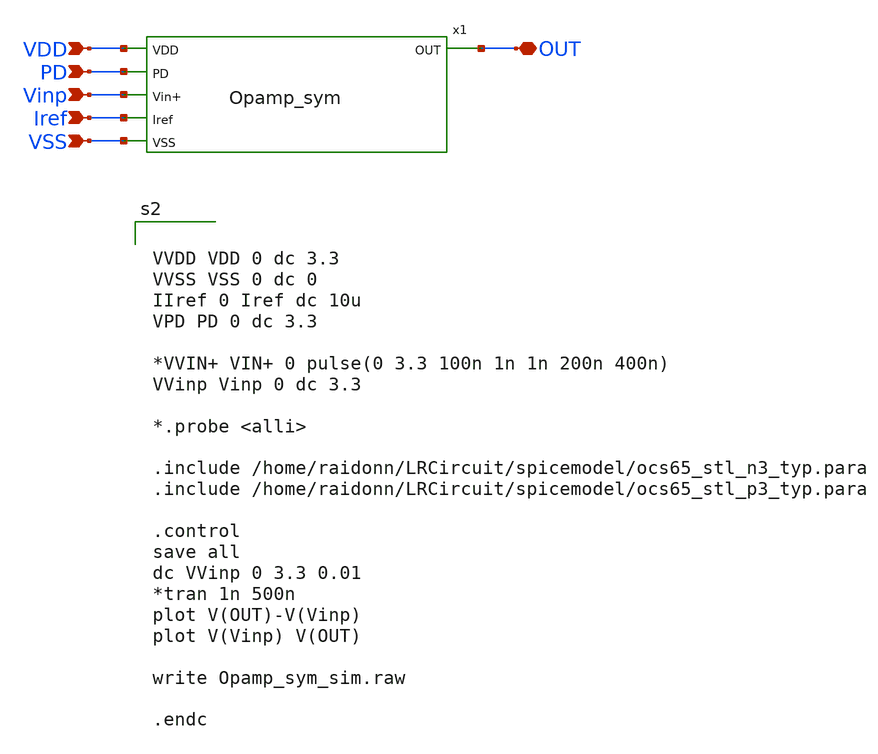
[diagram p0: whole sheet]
** sch_path: LR_Work4/Review_1112/sim/Opamp_sym_sim.sch
**.subckt Opamp_sym_sim VDD PD Vinp Iref VSS OUT
*.ipin VDD
*.ipin PD
*.ipin Vinp
*.ipin Iref
*.ipin VSS
*.iopin OUT
x1 VDD PD Vinp Iref VSS OUT Opamp_sym
**** begin user architecture code


VVDD VDD 0 dc 3.3
VVSS VSS 0 dc 0
IIref 0 Iref dc 10u
VPD PD 0 dc 3.3

*VVIN+ VIN+ 0 pulse(0 3.3 100n 1n 1n 200n 400n)
VVinp Vinp 0 dc 3.3

*.probe <alli>

.include /home/raidonn/LRCircuit/spicemodel/ocs65_stl_n3_typ.para
.include /home/raidonn/LRCircuit/spicemodel/ocs65_stl_p3_typ.para

.control
save all
dc VVinp 0 3.3 0.01
*tran 1n 500n
plot V(OUT)-V(Vinp)
plot V(Vinp) V(OUT)

write Opamp_sym_sim.raw

.endc

**** end user architecture code
**.ends
.end
